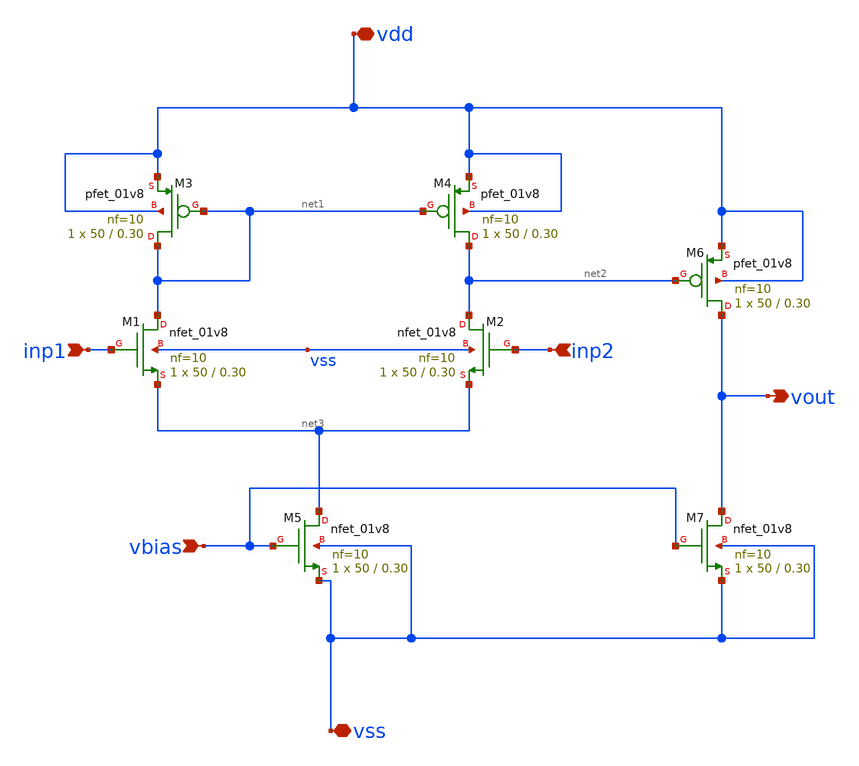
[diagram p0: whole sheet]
** sch_path: xschem/twostage_opamp.sch
**.subckt twostage_opamp inp1 inp2 vdd vss vbias vout
*.ipin inp1
*.ipin inp2
*.iopin vdd
*.iopin vss
*.ipin vbias
*.opin vout
XM1 net1 inp1 net3 vss sky130_fd_pr__nfet_01v8 L=0.30 W=50 nf=10 ad='int((nf+1)/2) * W/nf * 0.29' as='int((nf+2)/2) * W/nf * 0.29'
+ pd='2*int((nf+1)/2) * (W/nf + 0.29)' ps='2*int((nf+2)/2) * (W/nf + 0.29)' nrd='0.29 / W' nrs='0.29 / W'
+ sa=0 sb=0 sd=0 mult=1 m=1
XM2 net2 inp2 net3 vss sky130_fd_pr__nfet_01v8 L=0.30 W=50 nf=10 ad='int((nf+1)/2) * W/nf * 0.29' as='int((nf+2)/2) * W/nf * 0.29'
+ pd='2*int((nf+1)/2) * (W/nf + 0.29)' ps='2*int((nf+2)/2) * (W/nf + 0.29)' nrd='0.29 / W' nrs='0.29 / W'
+ sa=0 sb=0 sd=0 mult=1 m=1
XM3 net1 net1 vdd vdd sky130_fd_pr__pfet_01v8 L=0.30 W=50 nf=10 ad='int((nf+1)/2) * W/nf * 0.29' as='int((nf+2)/2) * W/nf * 0.29'
+ pd='2*int((nf+1)/2) * (W/nf + 0.29)' ps='2*int((nf+2)/2) * (W/nf + 0.29)' nrd='0.29 / W' nrs='0.29 / W'
+ sa=0 sb=0 sd=0 mult=1 m=1
XM5 net3 vbias vss vss sky130_fd_pr__nfet_01v8 L=0.30 W=50 nf=10 ad='int((nf+1)/2) * W/nf * 0.29' as='int((nf+2)/2) * W/nf * 0.29'
+ pd='2*int((nf+1)/2) * (W/nf + 0.29)' ps='2*int((nf+2)/2) * (W/nf + 0.29)' nrd='0.29 / W' nrs='0.29 / W'
+ sa=0 sb=0 sd=0 mult=1 m=1
XM7 vout vbias vss vss sky130_fd_pr__nfet_01v8 L=0.30 W=50 nf=10 ad='int((nf+1)/2) * W/nf * 0.29' as='int((nf+2)/2) * W/nf * 0.29'
+ pd='2*int((nf+1)/2) * (W/nf + 0.29)' ps='2*int((nf+2)/2) * (W/nf + 0.29)' nrd='0.29 / W' nrs='0.29 / W'
+ sa=0 sb=0 sd=0 mult=1 m=1
XM4 net2 net1 vdd vdd sky130_fd_pr__pfet_01v8 L=0.30 W=50 nf=10 ad='int((nf+1)/2) * W/nf * 0.29' as='int((nf+2)/2) * W/nf * 0.29'
+ pd='2*int((nf+1)/2) * (W/nf + 0.29)' ps='2*int((nf+2)/2) * (W/nf + 0.29)' nrd='0.29 / W' nrs='0.29 / W'
+ sa=0 sb=0 sd=0 mult=1 m=1
XM6 vout net2 vdd vdd sky130_fd_pr__pfet_01v8 L=0.30 W=50 nf=10 ad='int((nf+1)/2) * W/nf * 0.29' as='int((nf+2)/2) * W/nf * 0.29'
+ pd='2*int((nf+1)/2) * (W/nf + 0.29)' ps='2*int((nf+2)/2) * (W/nf + 0.29)' nrd='0.29 / W' nrs='0.29 / W'
+ sa=0 sb=0 sd=0 mult=1 m=1
**.ends
.end
